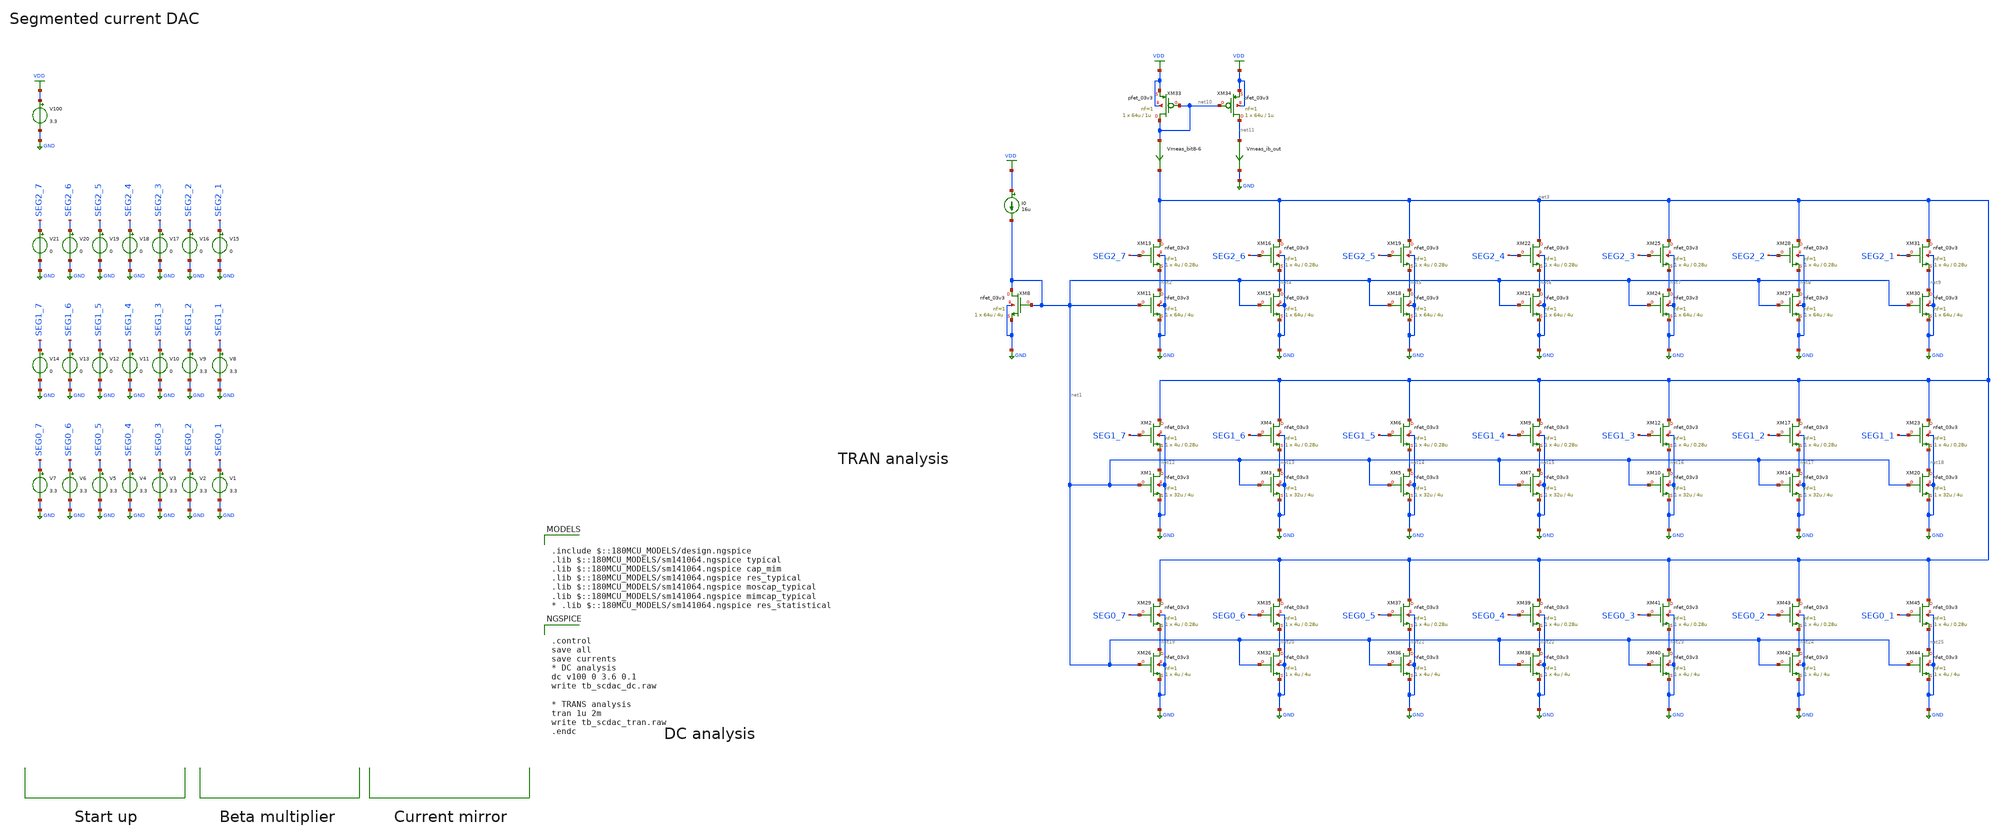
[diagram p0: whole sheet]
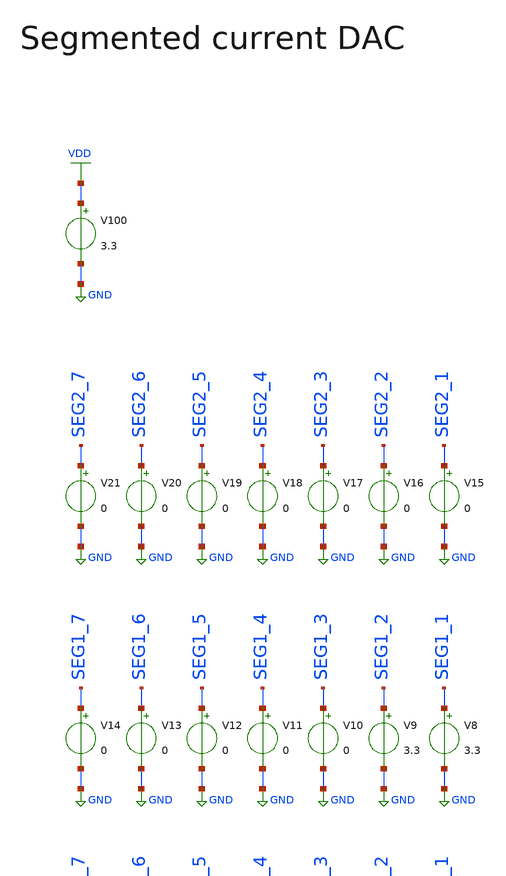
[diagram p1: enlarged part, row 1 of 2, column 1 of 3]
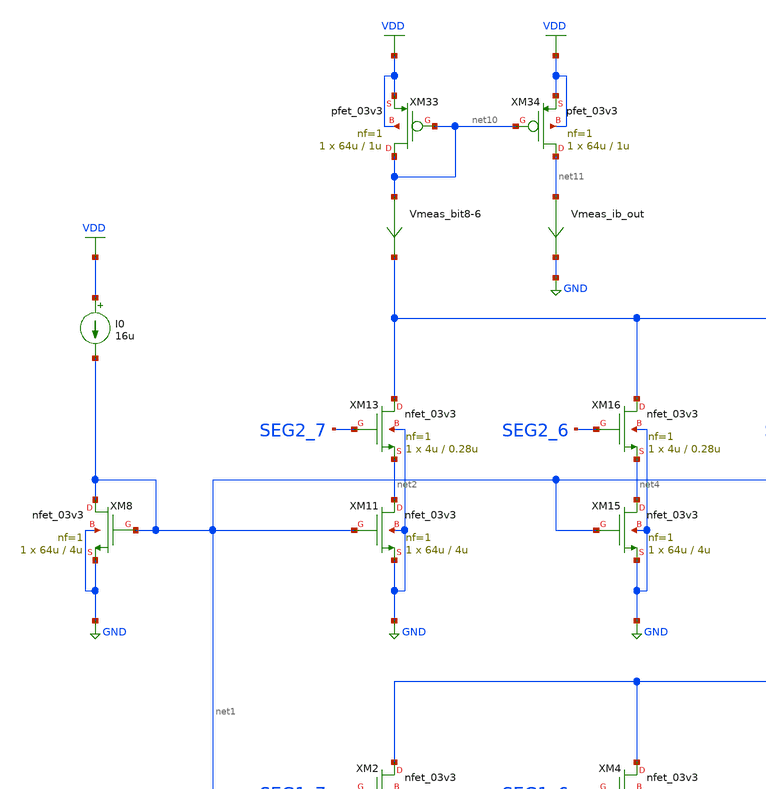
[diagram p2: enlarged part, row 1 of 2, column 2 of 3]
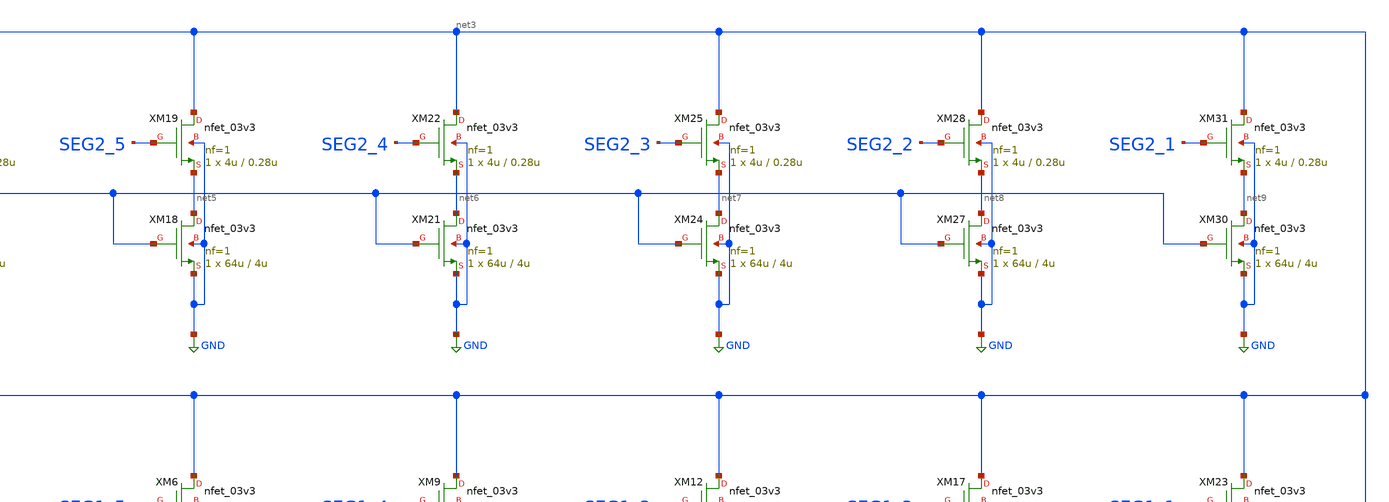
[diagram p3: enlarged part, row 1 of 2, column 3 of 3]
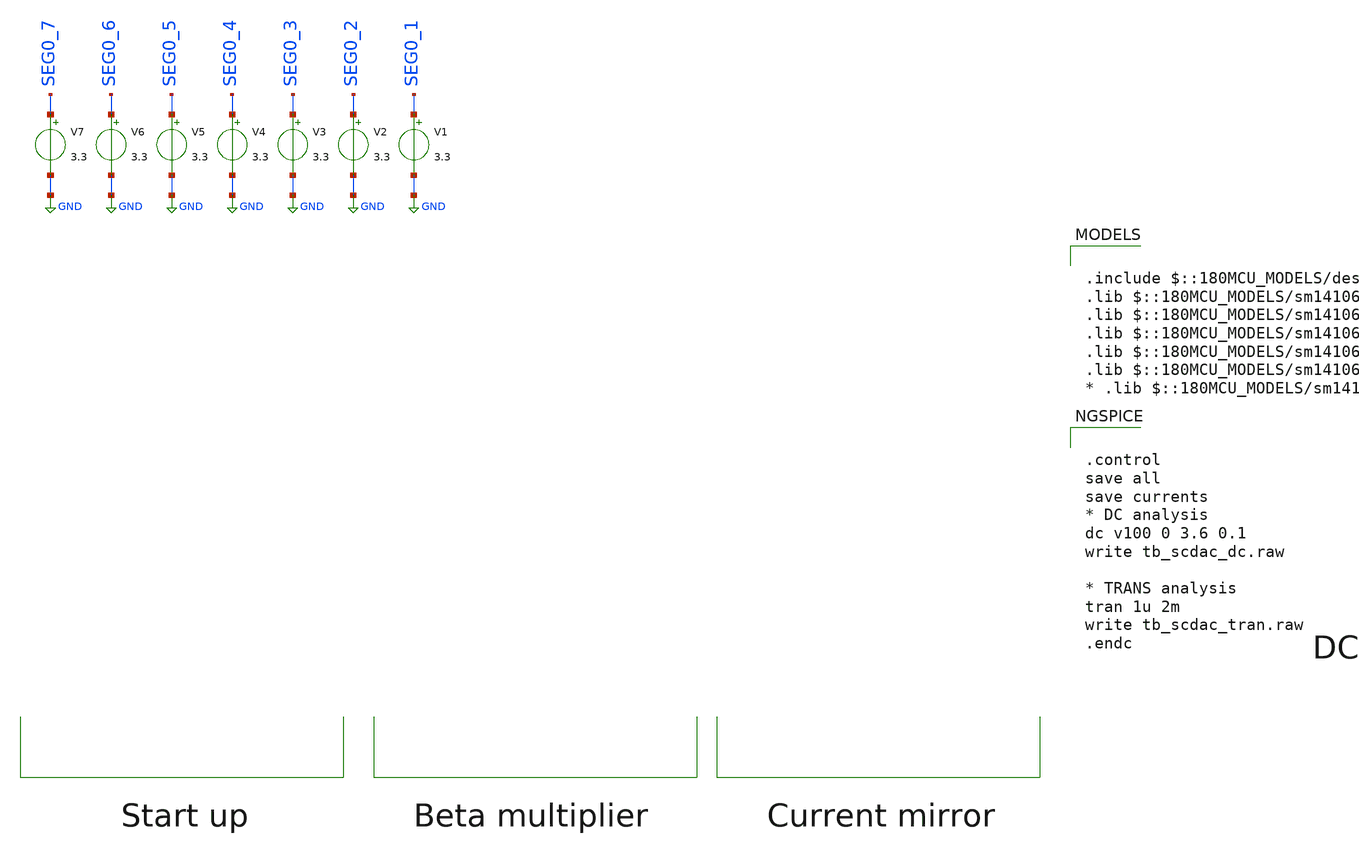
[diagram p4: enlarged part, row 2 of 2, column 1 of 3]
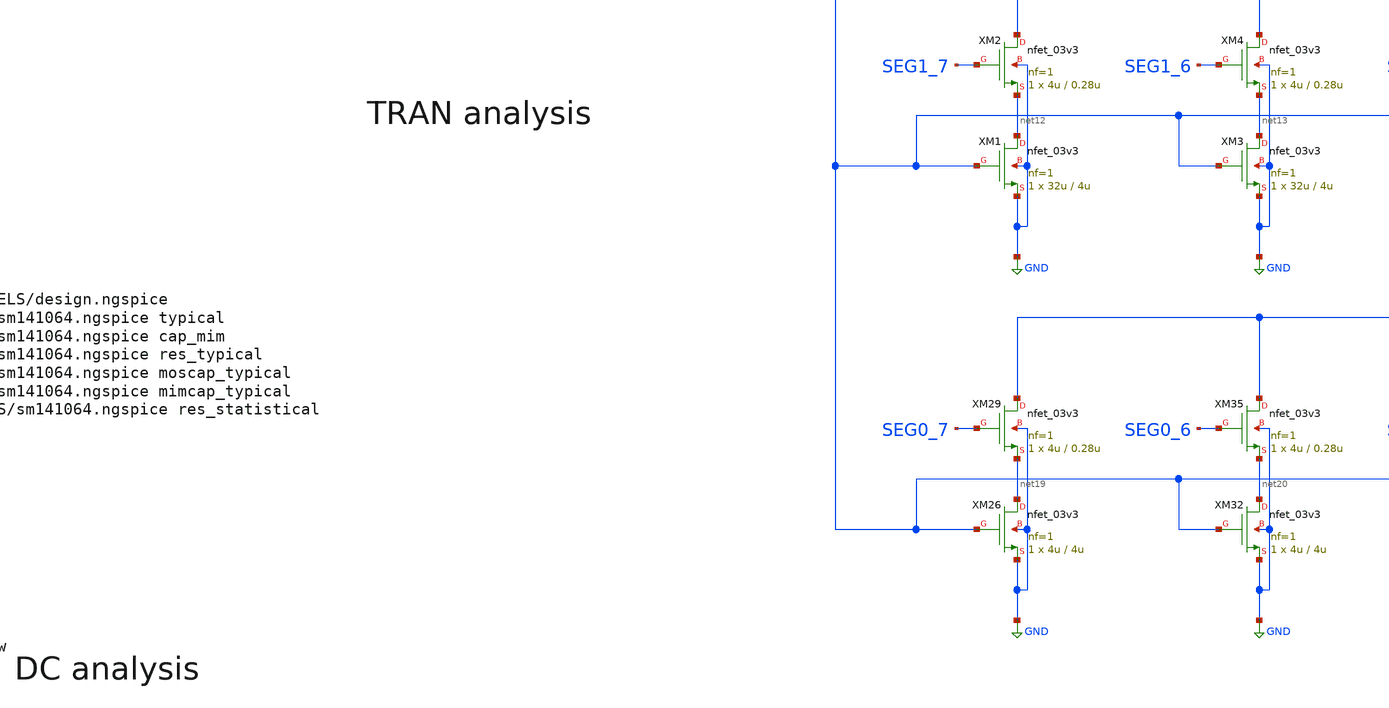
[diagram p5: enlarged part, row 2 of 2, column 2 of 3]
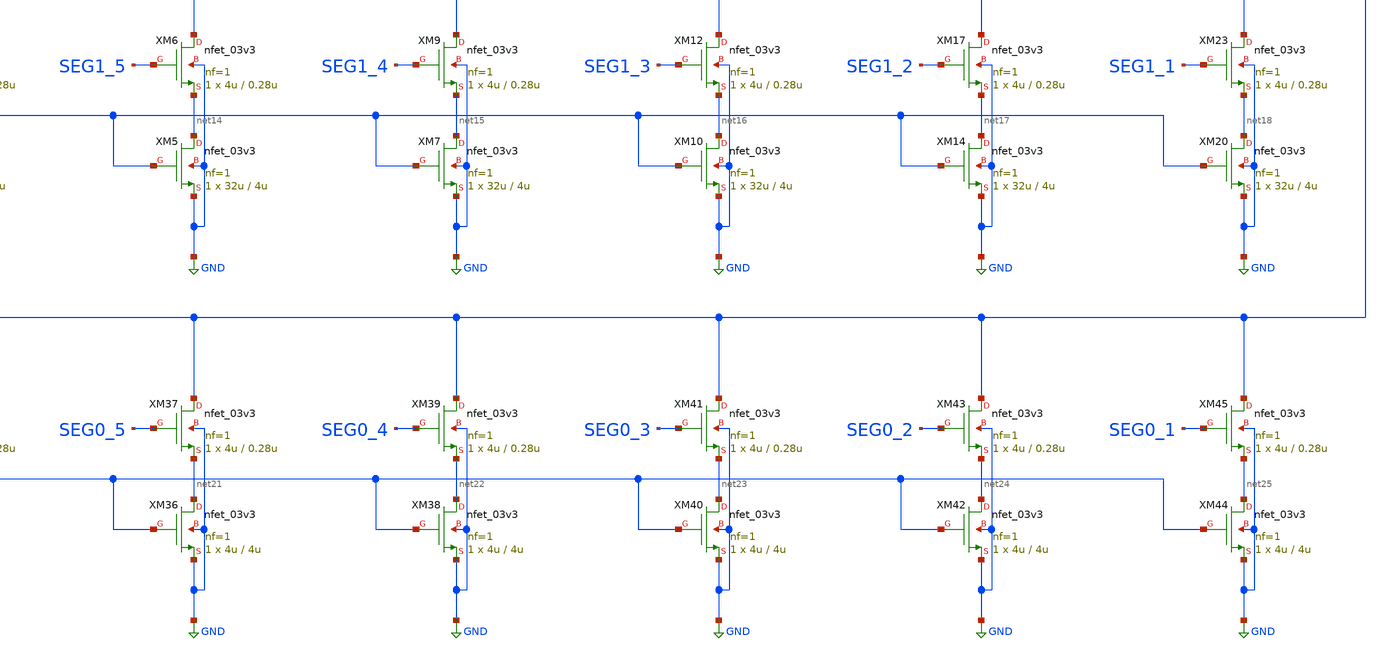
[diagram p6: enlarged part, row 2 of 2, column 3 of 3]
** sch_path: designs/libs/tb_analog/tb_scdac/tb_scdac.sch
* Copyright 2022 GlobalFoundries PDK Authors
* Licensed under the Apache License, Version 2.0 (the "License");
* you may not use this file except in compliance with the License.
* You may obtain a copy of the License at
* https://www.apache.org/licenses/LICENSE-2.0
* Unless required by applicable law or agreed to in writing, software
* distributed under the License is distributed on an "AS IS" BASIS,
* WITHOUT WARRANTIES OR CONDITIONS OF ANY KIND, either express or implied.
* See the License for the specific language governing permissions and
* limitations under the License.
**.subckt tb_scdac
V100 VDD GND 3.3
XM8 net1 net1 GND GND nfet_03v3 L=4u W=64u nf=1 ad='int((nf+1)/2) * W/nf * 0.18u' as='int((nf+2)/2) * W/nf * 0.18u'
+ pd='2*int((nf+1)/2) * (W/nf + 0.18u)' ps='2*int((nf+2)/2) * (W/nf + 0.18u)' nrd='0.18u / W' nrs='0.18u / W'
+ sa=0 sb=0 sd=0 m=1
I0 VDD net1 16u
XM11 net2 net1 GND GND nfet_03v3 L=4u W=64u nf=1 ad='int((nf+1)/2) * W/nf * 0.18u' as='int((nf+2)/2) * W/nf * 0.18u'
+ pd='2*int((nf+1)/2) * (W/nf + 0.18u)' ps='2*int((nf+2)/2) * (W/nf + 0.18u)' nrd='0.18u / W' nrs='0.18u / W'
+ sa=0 sb=0 sd=0 m=1
XM13 net3 SEG2_7 net2 GND nfet_03v3 L=0.28u W=4u nf=1 ad='int((nf+1)/2) * W/nf * 0.18u' as='int((nf+2)/2) * W/nf * 0.18u'
+ pd='2*int((nf+1)/2) * (W/nf + 0.18u)' ps='2*int((nf+2)/2) * (W/nf + 0.18u)' nrd='0.18u / W' nrs='0.18u / W'
+ sa=0 sb=0 sd=0 m=1
XM15 net4 net1 GND GND nfet_03v3 L=4u W=64u nf=1 ad='int((nf+1)/2) * W/nf * 0.18u' as='int((nf+2)/2) * W/nf * 0.18u'
+ pd='2*int((nf+1)/2) * (W/nf + 0.18u)' ps='2*int((nf+2)/2) * (W/nf + 0.18u)' nrd='0.18u / W' nrs='0.18u / W'
+ sa=0 sb=0 sd=0 m=1
XM16 net3 SEG2_6 net4 GND nfet_03v3 L=0.28u W=4u nf=1 ad='int((nf+1)/2) * W/nf * 0.18u' as='int((nf+2)/2) * W/nf * 0.18u'
+ pd='2*int((nf+1)/2) * (W/nf + 0.18u)' ps='2*int((nf+2)/2) * (W/nf + 0.18u)' nrd='0.18u / W' nrs='0.18u / W'
+ sa=0 sb=0 sd=0 m=1
XM18 net5 net1 GND GND nfet_03v3 L=4u W=64u nf=1 ad='int((nf+1)/2) * W/nf * 0.18u' as='int((nf+2)/2) * W/nf * 0.18u'
+ pd='2*int((nf+1)/2) * (W/nf + 0.18u)' ps='2*int((nf+2)/2) * (W/nf + 0.18u)' nrd='0.18u / W' nrs='0.18u / W'
+ sa=0 sb=0 sd=0 m=1
XM19 net3 SEG2_5 net5 GND nfet_03v3 L=0.28u W=4u nf=1 ad='int((nf+1)/2) * W/nf * 0.18u' as='int((nf+2)/2) * W/nf * 0.18u'
+ pd='2*int((nf+1)/2) * (W/nf + 0.18u)' ps='2*int((nf+2)/2) * (W/nf + 0.18u)' nrd='0.18u / W' nrs='0.18u / W'
+ sa=0 sb=0 sd=0 m=1
XM21 net6 net1 GND GND nfet_03v3 L=4u W=64u nf=1 ad='int((nf+1)/2) * W/nf * 0.18u' as='int((nf+2)/2) * W/nf * 0.18u'
+ pd='2*int((nf+1)/2) * (W/nf + 0.18u)' ps='2*int((nf+2)/2) * (W/nf + 0.18u)' nrd='0.18u / W' nrs='0.18u / W'
+ sa=0 sb=0 sd=0 m=1
XM22 net3 SEG2_4 net6 GND nfet_03v3 L=0.28u W=4u nf=1 ad='int((nf+1)/2) * W/nf * 0.18u' as='int((nf+2)/2) * W/nf * 0.18u'
+ pd='2*int((nf+1)/2) * (W/nf + 0.18u)' ps='2*int((nf+2)/2) * (W/nf + 0.18u)' nrd='0.18u / W' nrs='0.18u / W'
+ sa=0 sb=0 sd=0 m=1
XM24 net7 net1 GND GND nfet_03v3 L=4u W=64u nf=1 ad='int((nf+1)/2) * W/nf * 0.18u' as='int((nf+2)/2) * W/nf * 0.18u'
+ pd='2*int((nf+1)/2) * (W/nf + 0.18u)' ps='2*int((nf+2)/2) * (W/nf + 0.18u)' nrd='0.18u / W' nrs='0.18u / W'
+ sa=0 sb=0 sd=0 m=1
XM25 net3 SEG2_3 net7 GND nfet_03v3 L=0.28u W=4u nf=1 ad='int((nf+1)/2) * W/nf * 0.18u' as='int((nf+2)/2) * W/nf * 0.18u'
+ pd='2*int((nf+1)/2) * (W/nf + 0.18u)' ps='2*int((nf+2)/2) * (W/nf + 0.18u)' nrd='0.18u / W' nrs='0.18u / W'
+ sa=0 sb=0 sd=0 m=1
XM27 net8 net1 GND GND nfet_03v3 L=4u W=64u nf=1 ad='int((nf+1)/2) * W/nf * 0.18u' as='int((nf+2)/2) * W/nf * 0.18u'
+ pd='2*int((nf+1)/2) * (W/nf + 0.18u)' ps='2*int((nf+2)/2) * (W/nf + 0.18u)' nrd='0.18u / W' nrs='0.18u / W'
+ sa=0 sb=0 sd=0 m=1
XM28 net3 SEG2_2 net8 GND nfet_03v3 L=0.28u W=4u nf=1 ad='int((nf+1)/2) * W/nf * 0.18u' as='int((nf+2)/2) * W/nf * 0.18u'
+ pd='2*int((nf+1)/2) * (W/nf + 0.18u)' ps='2*int((nf+2)/2) * (W/nf + 0.18u)' nrd='0.18u / W' nrs='0.18u / W'
+ sa=0 sb=0 sd=0 m=1
XM30 net9 net1 GND GND nfet_03v3 L=4u W=64u nf=1 ad='int((nf+1)/2) * W/nf * 0.18u' as='int((nf+2)/2) * W/nf * 0.18u'
+ pd='2*int((nf+1)/2) * (W/nf + 0.18u)' ps='2*int((nf+2)/2) * (W/nf + 0.18u)' nrd='0.18u / W' nrs='0.18u / W'
+ sa=0 sb=0 sd=0 m=1
XM31 net3 SEG2_1 net9 GND nfet_03v3 L=0.28u W=4u nf=1 ad='int((nf+1)/2) * W/nf * 0.18u' as='int((nf+2)/2) * W/nf * 0.18u'
+ pd='2*int((nf+1)/2) * (W/nf + 0.18u)' ps='2*int((nf+2)/2) * (W/nf + 0.18u)' nrd='0.18u / W' nrs='0.18u / W'
+ sa=0 sb=0 sd=0 m=1
XM33 net10 net10 VDD VDD pfet_03v3 L=1u W=64u nf=1 ad='int((nf+1)/2) * W/nf * 0.18u' as='int((nf+2)/2) * W/nf * 0.18u'
+ pd='2*int((nf+1)/2) * (W/nf + 0.18u)' ps='2*int((nf+2)/2) * (W/nf + 0.18u)' nrd='0.18u / W' nrs='0.18u / W'
+ sa=0 sb=0 sd=0 m=1
XM34 net11 net10 VDD VDD pfet_03v3 L=1u W=64u nf=1 ad='int((nf+1)/2) * W/nf * 0.18u' as='int((nf+2)/2) * W/nf * 0.18u'
+ pd='2*int((nf+1)/2) * (W/nf + 0.18u)' ps='2*int((nf+2)/2) * (W/nf + 0.18u)' nrd='0.18u / W' nrs='0.18u / W'
+ sa=0 sb=0 sd=0 m=1
Vmeas_bit8-6 net10 net3 0
.save i(vmeas_bit8-6)
Vmeas_ib_out net11 GND 0
.save i(vmeas_ib_out)
XM1 net12 net1 GND GND nfet_03v3 L=4u W=32u nf=1 ad='int((nf+1)/2) * W/nf * 0.18u' as='int((nf+2)/2) * W/nf * 0.18u'
+ pd='2*int((nf+1)/2) * (W/nf + 0.18u)' ps='2*int((nf+2)/2) * (W/nf + 0.18u)' nrd='0.18u / W' nrs='0.18u / W'
+ sa=0 sb=0 sd=0 m=1
XM2 net3 SEG1_7 net12 GND nfet_03v3 L=0.28u W=4u nf=1 ad='int((nf+1)/2) * W/nf * 0.18u' as='int((nf+2)/2) * W/nf * 0.18u'
+ pd='2*int((nf+1)/2) * (W/nf + 0.18u)' ps='2*int((nf+2)/2) * (W/nf + 0.18u)' nrd='0.18u / W' nrs='0.18u / W'
+ sa=0 sb=0 sd=0 m=1
XM3 net13 net1 GND GND nfet_03v3 L=4u W=32u nf=1 ad='int((nf+1)/2) * W/nf * 0.18u' as='int((nf+2)/2) * W/nf * 0.18u'
+ pd='2*int((nf+1)/2) * (W/nf + 0.18u)' ps='2*int((nf+2)/2) * (W/nf + 0.18u)' nrd='0.18u / W' nrs='0.18u / W'
+ sa=0 sb=0 sd=0 m=1
XM4 net3 SEG1_6 net13 GND nfet_03v3 L=0.28u W=4u nf=1 ad='int((nf+1)/2) * W/nf * 0.18u' as='int((nf+2)/2) * W/nf * 0.18u'
+ pd='2*int((nf+1)/2) * (W/nf + 0.18u)' ps='2*int((nf+2)/2) * (W/nf + 0.18u)' nrd='0.18u / W' nrs='0.18u / W'
+ sa=0 sb=0 sd=0 m=1
XM5 net14 net1 GND GND nfet_03v3 L=4u W=32u nf=1 ad='int((nf+1)/2) * W/nf * 0.18u' as='int((nf+2)/2) * W/nf * 0.18u'
+ pd='2*int((nf+1)/2) * (W/nf + 0.18u)' ps='2*int((nf+2)/2) * (W/nf + 0.18u)' nrd='0.18u / W' nrs='0.18u / W'
+ sa=0 sb=0 sd=0 m=1
XM6 net3 SEG1_5 net14 GND nfet_03v3 L=0.28u W=4u nf=1 ad='int((nf+1)/2) * W/nf * 0.18u' as='int((nf+2)/2) * W/nf * 0.18u'
+ pd='2*int((nf+1)/2) * (W/nf + 0.18u)' ps='2*int((nf+2)/2) * (W/nf + 0.18u)' nrd='0.18u / W' nrs='0.18u / W'
+ sa=0 sb=0 sd=0 m=1
XM7 net15 net1 GND GND nfet_03v3 L=4u W=32u nf=1 ad='int((nf+1)/2) * W/nf * 0.18u' as='int((nf+2)/2) * W/nf * 0.18u'
+ pd='2*int((nf+1)/2) * (W/nf + 0.18u)' ps='2*int((nf+2)/2) * (W/nf + 0.18u)' nrd='0.18u / W' nrs='0.18u / W'
+ sa=0 sb=0 sd=0 m=1
XM9 net3 SEG1_4 net15 GND nfet_03v3 L=0.28u W=4u nf=1 ad='int((nf+1)/2) * W/nf * 0.18u' as='int((nf+2)/2) * W/nf * 0.18u'
+ pd='2*int((nf+1)/2) * (W/nf + 0.18u)' ps='2*int((nf+2)/2) * (W/nf + 0.18u)' nrd='0.18u / W' nrs='0.18u / W'
+ sa=0 sb=0 sd=0 m=1
XM10 net16 net1 GND GND nfet_03v3 L=4u W=32u nf=1 ad='int((nf+1)/2) * W/nf * 0.18u' as='int((nf+2)/2) * W/nf * 0.18u'
+ pd='2*int((nf+1)/2) * (W/nf + 0.18u)' ps='2*int((nf+2)/2) * (W/nf + 0.18u)' nrd='0.18u / W' nrs='0.18u / W'
+ sa=0 sb=0 sd=0 m=1
XM12 net3 SEG1_3 net16 GND nfet_03v3 L=0.28u W=4u nf=1 ad='int((nf+1)/2) * W/nf * 0.18u' as='int((nf+2)/2) * W/nf * 0.18u'
+ pd='2*int((nf+1)/2) * (W/nf + 0.18u)' ps='2*int((nf+2)/2) * (W/nf + 0.18u)' nrd='0.18u / W' nrs='0.18u / W'
+ sa=0 sb=0 sd=0 m=1
XM14 net17 net1 GND GND nfet_03v3 L=4u W=32u nf=1 ad='int((nf+1)/2) * W/nf * 0.18u' as='int((nf+2)/2) * W/nf * 0.18u'
+ pd='2*int((nf+1)/2) * (W/nf + 0.18u)' ps='2*int((nf+2)/2) * (W/nf + 0.18u)' nrd='0.18u / W' nrs='0.18u / W'
+ sa=0 sb=0 sd=0 m=1
XM17 net3 SEG1_2 net17 GND nfet_03v3 L=0.28u W=4u nf=1 ad='int((nf+1)/2) * W/nf * 0.18u' as='int((nf+2)/2) * W/nf * 0.18u'
+ pd='2*int((nf+1)/2) * (W/nf + 0.18u)' ps='2*int((nf+2)/2) * (W/nf + 0.18u)' nrd='0.18u / W' nrs='0.18u / W'
+ sa=0 sb=0 sd=0 m=1
XM20 net18 net1 GND GND nfet_03v3 L=4u W=32u nf=1 ad='int((nf+1)/2) * W/nf * 0.18u' as='int((nf+2)/2) * W/nf * 0.18u'
+ pd='2*int((nf+1)/2) * (W/nf + 0.18u)' ps='2*int((nf+2)/2) * (W/nf + 0.18u)' nrd='0.18u / W' nrs='0.18u / W'
+ sa=0 sb=0 sd=0 m=1
XM23 net3 SEG1_1 net18 GND nfet_03v3 L=0.28u W=4u nf=1 ad='int((nf+1)/2) * W/nf * 0.18u' as='int((nf+2)/2) * W/nf * 0.18u'
+ pd='2*int((nf+1)/2) * (W/nf + 0.18u)' ps='2*int((nf+2)/2) * (W/nf + 0.18u)' nrd='0.18u / W' nrs='0.18u / W'
+ sa=0 sb=0 sd=0 m=1
XM26 net19 net1 GND GND nfet_03v3 L=4u W=4u nf=1 ad='int((nf+1)/2) * W/nf * 0.18u' as='int((nf+2)/2) * W/nf * 0.18u'
+ pd='2*int((nf+1)/2) * (W/nf + 0.18u)' ps='2*int((nf+2)/2) * (W/nf + 0.18u)' nrd='0.18u / W' nrs='0.18u / W'
+ sa=0 sb=0 sd=0 m=1
XM29 net3 SEG0_7 net19 GND nfet_03v3 L=0.28u W=4u nf=1 ad='int((nf+1)/2) * W/nf * 0.18u' as='int((nf+2)/2) * W/nf * 0.18u'
+ pd='2*int((nf+1)/2) * (W/nf + 0.18u)' ps='2*int((nf+2)/2) * (W/nf + 0.18u)' nrd='0.18u / W' nrs='0.18u / W'
+ sa=0 sb=0 sd=0 m=1
XM32 net20 net1 GND GND nfet_03v3 L=4u W=4u nf=1 ad='int((nf+1)/2) * W/nf * 0.18u' as='int((nf+2)/2) * W/nf * 0.18u'
+ pd='2*int((nf+1)/2) * (W/nf + 0.18u)' ps='2*int((nf+2)/2) * (W/nf + 0.18u)' nrd='0.18u / W' nrs='0.18u / W'
+ sa=0 sb=0 sd=0 m=1
XM35 net3 SEG0_6 net20 GND nfet_03v3 L=0.28u W=4u nf=1 ad='int((nf+1)/2) * W/nf * 0.18u' as='int((nf+2)/2) * W/nf * 0.18u'
+ pd='2*int((nf+1)/2) * (W/nf + 0.18u)' ps='2*int((nf+2)/2) * (W/nf + 0.18u)' nrd='0.18u / W' nrs='0.18u / W'
+ sa=0 sb=0 sd=0 m=1
XM36 net21 net1 GND GND nfet_03v3 L=4u W=4u nf=1 ad='int((nf+1)/2) * W/nf * 0.18u' as='int((nf+2)/2) * W/nf * 0.18u'
+ pd='2*int((nf+1)/2) * (W/nf + 0.18u)' ps='2*int((nf+2)/2) * (W/nf + 0.18u)' nrd='0.18u / W' nrs='0.18u / W'
+ sa=0 sb=0 sd=0 m=1
XM37 net3 SEG0_5 net21 GND nfet_03v3 L=0.28u W=4u nf=1 ad='int((nf+1)/2) * W/nf * 0.18u' as='int((nf+2)/2) * W/nf * 0.18u'
+ pd='2*int((nf+1)/2) * (W/nf + 0.18u)' ps='2*int((nf+2)/2) * (W/nf + 0.18u)' nrd='0.18u / W' nrs='0.18u / W'
+ sa=0 sb=0 sd=0 m=1
XM38 net22 net1 GND GND nfet_03v3 L=4u W=4u nf=1 ad='int((nf+1)/2) * W/nf * 0.18u' as='int((nf+2)/2) * W/nf * 0.18u'
+ pd='2*int((nf+1)/2) * (W/nf + 0.18u)' ps='2*int((nf+2)/2) * (W/nf + 0.18u)' nrd='0.18u / W' nrs='0.18u / W'
+ sa=0 sb=0 sd=0 m=1
XM39 net3 SEG0_4 net22 GND nfet_03v3 L=0.28u W=4u nf=1 ad='int((nf+1)/2) * W/nf * 0.18u' as='int((nf+2)/2) * W/nf * 0.18u'
+ pd='2*int((nf+1)/2) * (W/nf + 0.18u)' ps='2*int((nf+2)/2) * (W/nf + 0.18u)' nrd='0.18u / W' nrs='0.18u / W'
+ sa=0 sb=0 sd=0 m=1
XM40 net23 net1 GND GND nfet_03v3 L=4u W=4u nf=1 ad='int((nf+1)/2) * W/nf * 0.18u' as='int((nf+2)/2) * W/nf * 0.18u'
+ pd='2*int((nf+1)/2) * (W/nf + 0.18u)' ps='2*int((nf+2)/2) * (W/nf + 0.18u)' nrd='0.18u / W' nrs='0.18u / W'
+ sa=0 sb=0 sd=0 m=1
XM41 net3 SEG0_3 net23 GND nfet_03v3 L=0.28u W=4u nf=1 ad='int((nf+1)/2) * W/nf * 0.18u' as='int((nf+2)/2) * W/nf * 0.18u'
+ pd='2*int((nf+1)/2) * (W/nf + 0.18u)' ps='2*int((nf+2)/2) * (W/nf + 0.18u)' nrd='0.18u / W' nrs='0.18u / W'
+ sa=0 sb=0 sd=0 m=1
XM42 net24 net1 GND GND nfet_03v3 L=4u W=4u nf=1 ad='int((nf+1)/2) * W/nf * 0.18u' as='int((nf+2)/2) * W/nf * 0.18u'
+ pd='2*int((nf+1)/2) * (W/nf + 0.18u)' ps='2*int((nf+2)/2) * (W/nf + 0.18u)' nrd='0.18u / W' nrs='0.18u / W'
+ sa=0 sb=0 sd=0 m=1
XM43 net3 SEG0_2 net24 GND nfet_03v3 L=0.28u W=4u nf=1 ad='int((nf+1)/2) * W/nf * 0.18u' as='int((nf+2)/2) * W/nf * 0.18u'
+ pd='2*int((nf+1)/2) * (W/nf + 0.18u)' ps='2*int((nf+2)/2) * (W/nf + 0.18u)' nrd='0.18u / W' nrs='0.18u / W'
+ sa=0 sb=0 sd=0 m=1
XM44 net25 net1 GND GND nfet_03v3 L=4u W=4u nf=1 ad='int((nf+1)/2) * W/nf * 0.18u' as='int((nf+2)/2) * W/nf * 0.18u'
+ pd='2*int((nf+1)/2) * (W/nf + 0.18u)' ps='2*int((nf+2)/2) * (W/nf + 0.18u)' nrd='0.18u / W' nrs='0.18u / W'
+ sa=0 sb=0 sd=0 m=1
XM45 net3 SEG0_1 net25 GND nfet_03v3 L=0.28u W=4u nf=1 ad='int((nf+1)/2) * W/nf * 0.18u' as='int((nf+2)/2) * W/nf * 0.18u'
+ pd='2*int((nf+1)/2) * (W/nf + 0.18u)' ps='2*int((nf+2)/2) * (W/nf + 0.18u)' nrd='0.18u / W' nrs='0.18u / W'
+ sa=0 sb=0 sd=0 m=1
V21 SEG2_7 GND 0
V20 SEG2_6 GND 0
V19 SEG2_5 GND 0
V18 SEG2_4 GND 0
V17 SEG2_3 GND 0
V16 SEG2_2 GND 0
V15 SEG2_1 GND 0
V14 SEG1_7 GND 0
V13 SEG1_6 GND 0
V12 SEG1_5 GND 0
V11 SEG1_4 GND 0
V10 SEG1_3 GND 0
V9 SEG1_2 GND 3.3
V8 SEG1_1 GND 3.3
V7 SEG0_7 GND 3.3
V6 SEG0_6 GND 3.3
V5 SEG0_5 GND 3.3
V4 SEG0_4 GND 3.3
V3 SEG0_3 GND 3.3
V2 SEG0_2 GND 3.3
V1 SEG0_1 GND 3.3
**** begin user architecture code


.control
save all
save currents
* DC analysis
dc v100 0 3.6 0.1
write tb_scdac_dc.raw

* TRANS analysis
tran 1u 2m
write tb_scdac_tran.raw
.endc



.include $::180MCU_MODELS/design.ngspice
.lib $::180MCU_MODELS/sm141064.ngspice typical
.lib $::180MCU_MODELS/sm141064.ngspice cap_mim
.lib $::180MCU_MODELS/sm141064.ngspice res_typical
.lib $::180MCU_MODELS/sm141064.ngspice moscap_typical
.lib $::180MCU_MODELS/sm141064.ngspice mimcap_typical
* .lib $::180MCU_MODELS/sm141064.ngspice res_statistical

**** end user architecture code
**.ends
.GLOBAL VDD
.GLOBAL GND
.end
